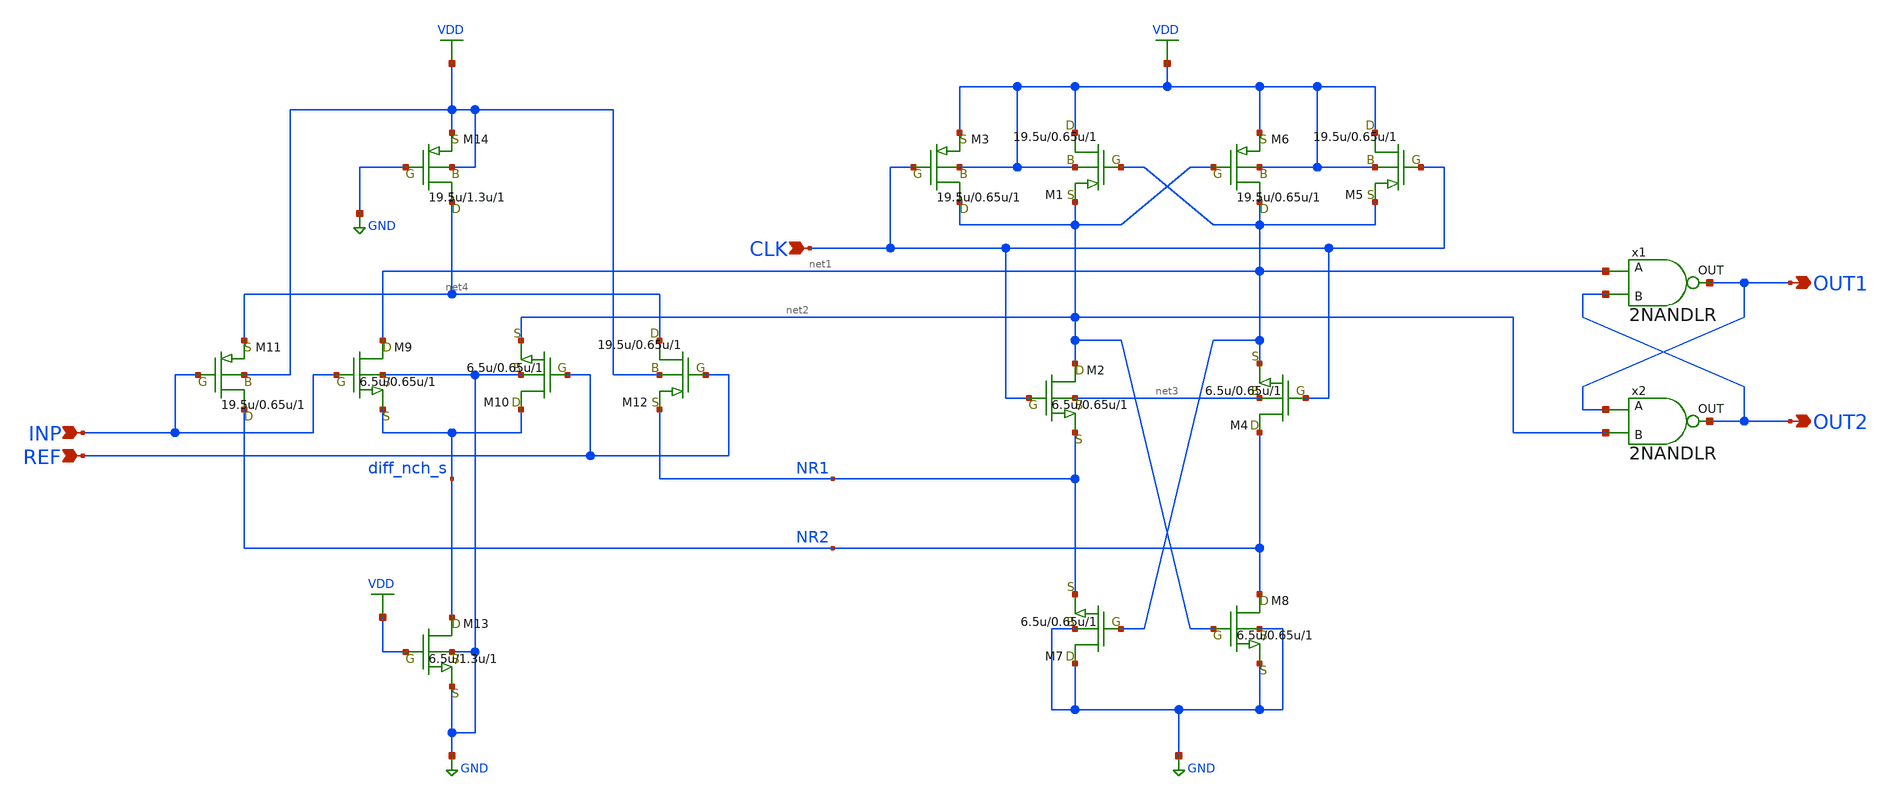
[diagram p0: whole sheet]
** sch_path: LR_hokari/LR_Work2/Wide-swing_clocked_comparator.sch
**.subckt Wide-swing_clocked_comparator INP REF CLK OUT1 OUT2
*.ipin INP
*.ipin REF
*.ipin CLK
*.opin OUT1
*.opin OUT2
M2 net2 CLK NR1 net3 nch w=6.5u l=0.65u as=0 ps=0 ad=0 pd=0 m=1
M4 NR2 CLK net1 net3 nch w=6.5u l=0.65u as=0 ps=0 ad=0 pd=0 m=1
M5 VDD CLK net1 VDD pch w=19.5u l=0.65u as=0 ps=0 ad=0 pd=0 m=1
M6 net1 net2 VDD VDD pch w=19.5u l=0.65u as=0 ps=0 ad=0 pd=0 m=1
M7 GND net1 NR1 GND nch w=6.5u l=0.65u as=0 ps=0 ad=0 pd=0 m=1
M8 NR2 net2 GND GND nch w=6.5u l=0.65u as=0 ps=0 ad=0 pd=0 m=1
x1 net1 OUT1 OUT2 2NANDLR
x2 OUT1 OUT2 net2 2NANDLR
M1 VDD net1 net2 VDD pch w=19.5u l=0.65u as=0 ps=0 ad=0 pd=0 m=1
M3 net2 CLK VDD VDD pch w=19.5u l=0.65u as=0 ps=0 ad=0 pd=0 m=1
M12 net4 REF NR1 VDD pch w=19.5u l=0.65u as=0 ps=0 ad=0 pd=0 m=1
M11 NR2 INP net4 VDD pch w=19.5u l=0.65u as=0 ps=0 ad=0 pd=0 m=1
M9 net1 INP diff_nch_s GND nch w=6.5u l=0.65u as=0 ps=0 ad=0 pd=0 m=1
M10 diff_nch_s REF net2 GND nch w=6.5u l=0.65u as=0 ps=0 ad=0 pd=0 m=1
M13 diff_nch_s VDD GND GND nch w=6.5u l=1.3u as=0 ps=0 ad=0 pd=0 m=1
M14 net4 GND VDD VDD pch w=19.5u l=1.3u as=0 ps=0 ad=0 pd=0 m=1
**** begin user architecture code



.inc /home/hnriv/LR_hokari/OCS65_model.para


VVDD VDD 0 DC 3.3

VINP INP 0 pwl (0 0 25n 0 26n 3.3 75n 3.3 76n 0.2 125n 0.2 126n 3.1 175n 3.1 176n 0.4 225n 0.4 226n
+ 2.9 275n 2.9 276n 0.6 325n 0.6 326n 2.7 375n 2.7 376n 0.8 425n 0.8 426n 2.5 475n 2.5 476n 1.0 525n 1.0
+ 526n 2.3 575n 2.3 576n 1.2 625n 1.2 626n 2.1 675n 2.1 676n 1.4 725n 1.4 726n 1.9 775n 1.9 776n 1.6 825n
+ 1.6 826n 1.7 875n 1.7)

*VINP INP 0 pwl (0 2.15 25n 2.15 26n 1.15 75n 1.15 76n 1.95 125n 1.95 126n 1.35 175n 1.35)
*VINP INP 0 pwl (0 1.85 25n 1.85 26n 1.45 75n 1.45 76n 1.83 125n 1.83 126n 1.47 175n 1.47)

VREF REF 0 DC 1.65

VCLK CLK 0 pulse(0 3.3 0 1p 1p 12.5n 50n)

.control
tran 1n 875n

meas tran delayIN1 find time WHEN v(CLK)=0.9 RISE=3
meas tran delayOUT find time WHEN v(OUT1)=0.9 FALL=2
let delay1 = delayOUT - delayIN1
echo tpHL = $&delay1

meas tran delayIN1 find time WHEN v(CLK)=0.9 RISE=4
meas tran delayOUT find time WHEN v(OUT1)=0.9 RISE=2
let delay2 = delayOUT - delayIN1
echo tpLH = $&delay2



plot v(OUT1)

write Wide-swing_clocked_comparator.raw

.endc

**** end user architecture code
**.ends

* expanding   symbol:  LR_Work2/symbol/2NANDLR.sym # of pins=3
** sym_path: LR_Work2/symbol/2NANDLR.sym
** sch_path: LR_Work2/symbol/2NANDLR.sch
.subckt 2NANDLR A OUT B
*.ipin A
*.ipin B
*.opin OUT
M1 OUT A net1 GND nch w=1u l=0.35u as=0 ps=0 ad=0 pd=0 m=1
M2 OUT B VDD VDD pch w=1u l=0.35u as=0 ps=0 ad=0 pd=0 m=1
M3 OUT A VDD VDD pch w=1u l=0.35u as=0 ps=0 ad=0 pd=0 m=1
M4 net1 B GND GND nch w=1u l=0.35u as=0 ps=0 ad=0 pd=0 m=1
.ends

.GLOBAL VDD
.GLOBAL GND
.end
